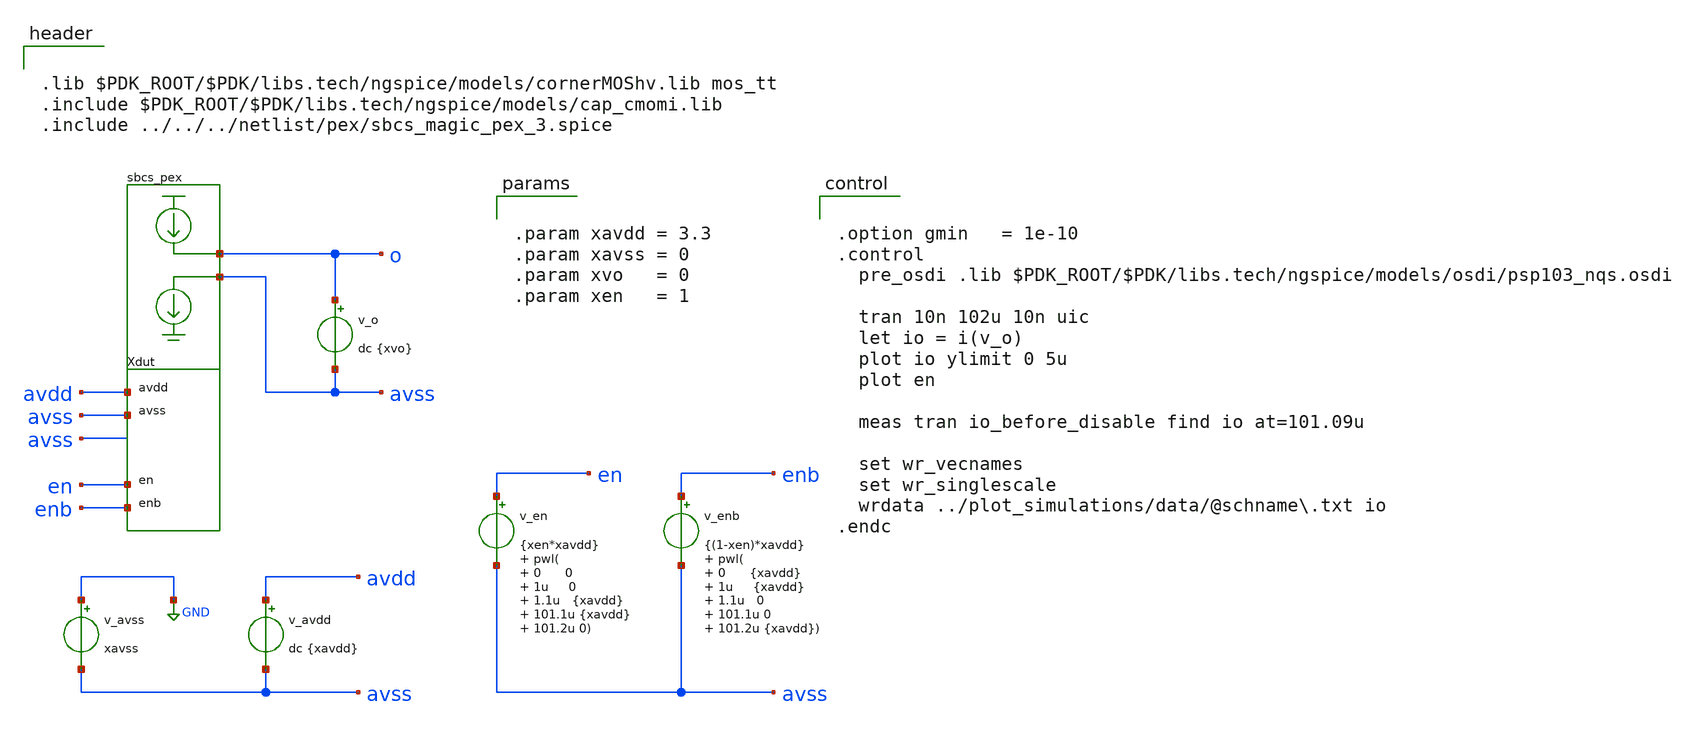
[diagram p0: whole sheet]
** sch_path: macros/sbcs/testbenches/xschem/pex_tb_sbcs_tran.sch
**.subckt pex_tb_sbcs_tran
Xdut o avss avdd avss en enb sbcs_pex
v_avss GND avss xavss
v_avdd avdd avss dc {xavdd}
v_en en avss {xen*xavdd} pwl( 0 0 1u 0 1.1u {xavdd} 101.1u {xavdd} 101.2u 0)
v_enb enb avss {(1-xen)*xavdd} pwl( 0 {xavdd} 1u {xavdd} 1.1u 0 101.1u 0 101.2u {xavdd})

v_o o avss dc {xvo}
**** begin user architecture code


.lib $PDK_ROOT/$PDK/libs.tech/ngspice/models/cornerMOShv.lib mos_tt
.include $PDK_ROOT/$PDK/libs.tech/ngspice/models/cap_cmomi.lib
.include ../../../netlist/pex/sbcs_magic_pex_3.spice




.option gmin   = 1e-10
.control
  pre_osdi .lib $PDK_ROOT/$PDK/libs.tech/ngspice/models/osdi/psp103_nqs.osdi

  tran 10n 102u 10n uic
  let io = i(v_o)
  plot io ylimit 0 5u
  plot en

  meas tran io_before_disable find io at=101.09u

  set wr_vecnames
  set wr_singlescale
  wrdata ../plot_simulations/data/@schname\.txt io
.endc




.param xavdd = 3.3
.param xavss = 0
.param xvo   = 0
.param xen   = 1


**** end user architecture code
**.ends
.GLOBAL GND
.end
